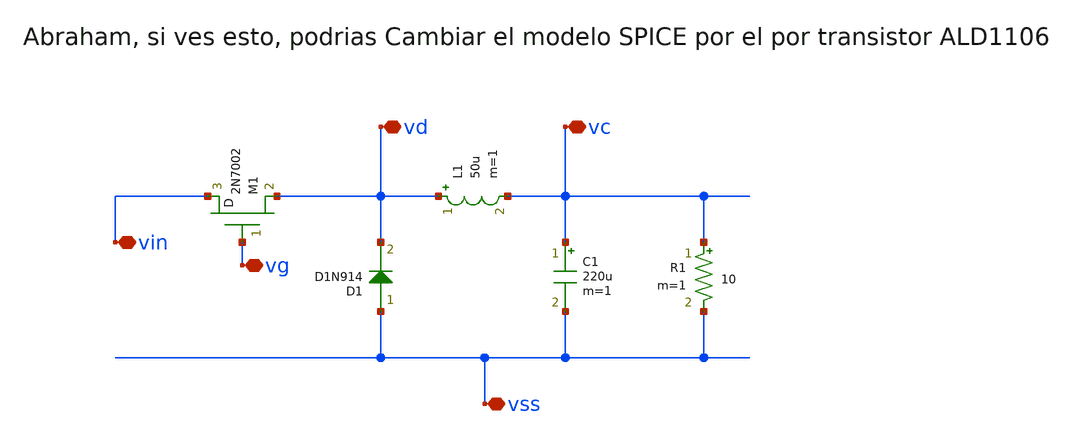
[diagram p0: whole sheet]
** sch_path: DC_DC/buck.sch
**.subckt buck vss vd vc vin vg
*.iopin vss
*.iopin vd
*.iopin vc
*.iopin vin
*.iopin vg
M1 vin vg vd M2N7002 m=1
D1 vss vd D1N914 area=1
L1 vd vc 50u m=1
C1 vc vss 220u m=1
R1 vc vss 10 m=1
**.ends
.end
